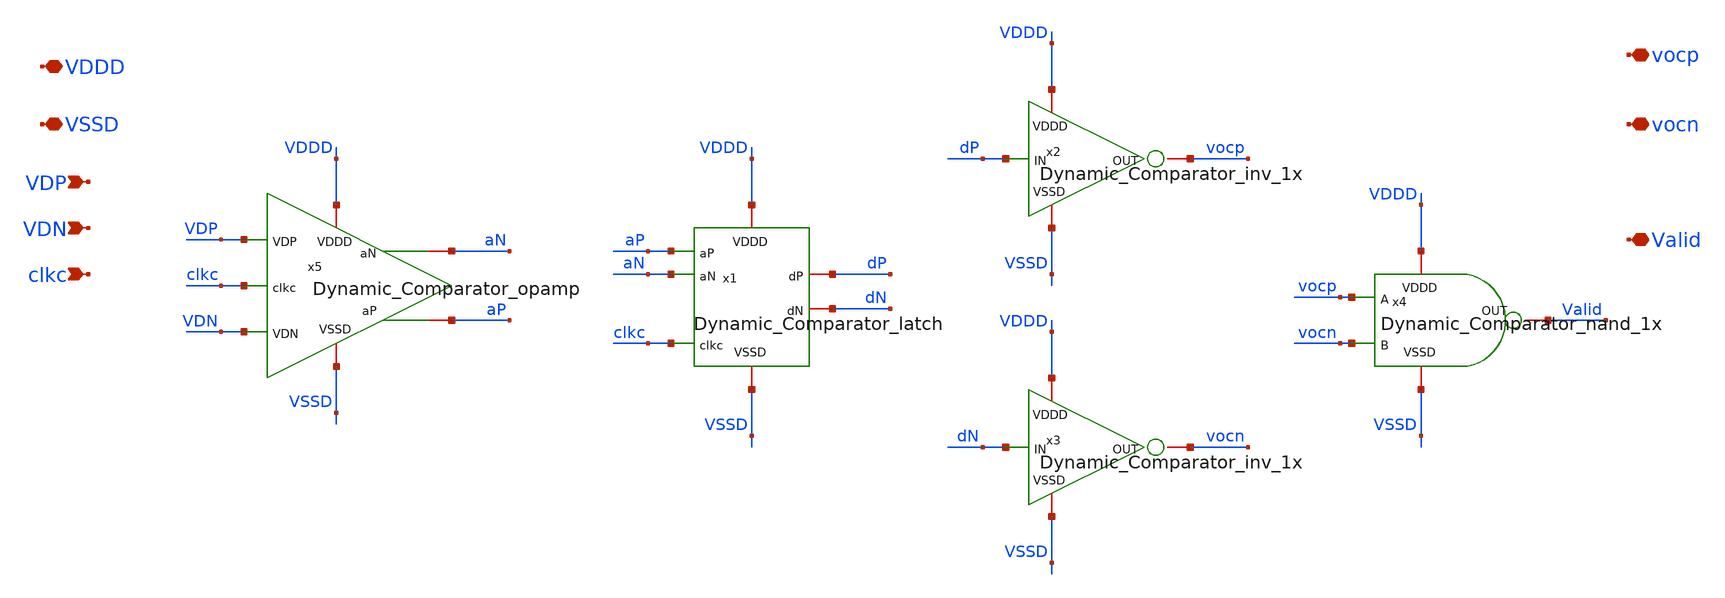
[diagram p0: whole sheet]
** sch_path: SAR_ADC/Dynamic_Comparator/xschem/Dynamic_Comparator.sch
**.subckt Dynamic_Comparator VDDD VSSD VDP VDN clkc Valid vocn vocp
*.iopin VDDD
*.iopin VSSD
*.ipin VDP
*.ipin VDN
*.ipin clkc
*.iopin Valid
*.iopin vocn
*.iopin vocp
x5 aN VDDD aP VSSD clkc VDP VDN Dynamic_Comparator_opamp
x1 VDDD VSSD dN clkc dP aP aN Dynamic_Comparator_latch
x2 VDDD VSSD vocp dP Dynamic_Comparator_inv_1x
x3 VDDD VSSD vocn dN Dynamic_Comparator_inv_1x
x4 VDDD VSSD Valid vocp vocn Dynamic_Comparator_nand_1x
**.ends
.end
